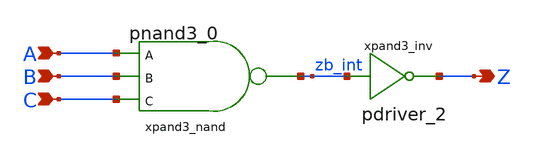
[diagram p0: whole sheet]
** sch_path: sram_4_16_scn4m/pand3_0.sch
**.subckt pand3_0 A B C Z
*.ipin A
*.ipin B
*.ipin C
*.opin Z
xpand3_nand A B C zb_int vdd gnd pnand3_0
xpand3_inv zb_int Z vdd gnd pdriver_2
**.ends

* expanding   symbol:  pnand3_0.sym # of pins=4
** sym_path: sram_4_16_scn4m/pnand3_0.sym
** sch_path: sram_4_16_scn4m/pnand3_0.sch
.subckt pnand3_0 A B C Z vdd gnd
*.ipin C
*.ipin A
*.ipin B
*.opin Z
*.iopin vdd
*.iopin gnd
Mpnand3_nmos1 Z C net1 gnd n w=1.6u l=0.4u m=1
Mpnand3_pmos1 Z A vdd vdd p w=1.6u l=0.4u m=1
Mpnand3_pmos3 Z C vdd vdd p w=1.6u l=0.4u m=1
Mpnand3_nmos2 net1 B net2 gnd n w=1.6u l=0.4u m=1
Mpnand3_pmos2 Z B vdd vdd p w=1.6u l=0.4u m=1
Mpnand3_nmos3 net2 A gnd gnd n w=1.6u l=0.4u m=1
.ends


* expanding   symbol:  pdriver_2.sym # of pins=2
** sym_path: sram_4_16_scn4m/pdriver_2.sym
** sch_path: sram_4_16_scn4m/pdriver_2.sch
.subckt pdriver_2 A Z vdd gnd
*.ipin A
*.opin Z
xbuf_inv1 A Z vdd gnd pinv_11
.ends


* expanding   symbol:  pinv_11.sym # of pins=2
** sym_path: sram_4_16_scn4m/pinv_11.sym
** sch_path: sram_4_16_scn4m/pinv_11.sch
.subckt pinv_11 A Z vdd gnd
*.ipin A
*.opin Z
*.iopin vdd
*.iopin gnd
M2 Z A gnd gnd n w=3.2u l=0.4u m=1
M3 Z A vdd vdd p w=6.4u l=0.4u m=1
.ends

.end
